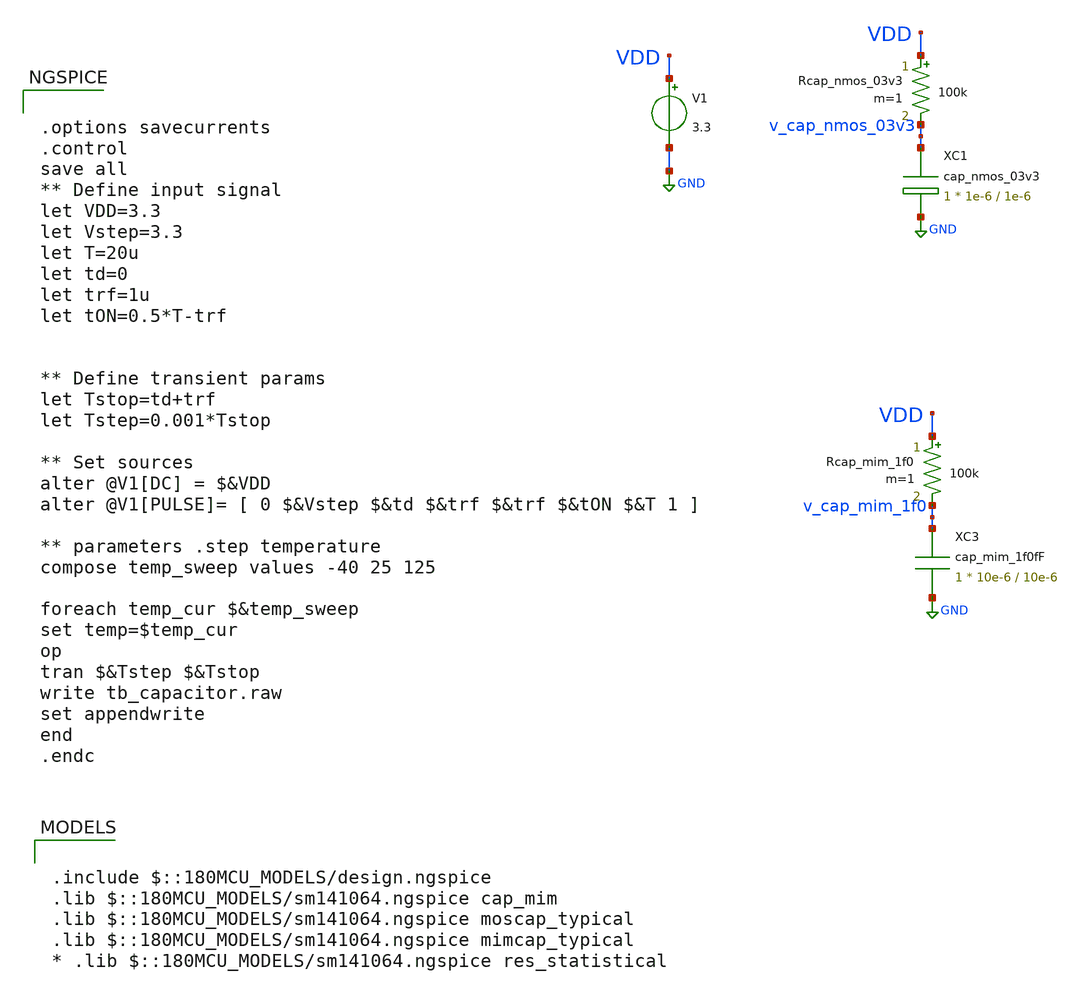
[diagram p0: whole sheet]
** sch_path: designs/libs/tb_analog/tb_capacitor/tb_capacitor.sch
**.subckt tb_capacitor
V1 VDD GND 3.3
XC1 v_cap_nmos_03v3 GND cap_nmos_03v3 c_width=1e-6 c_length=1e-6 m=1
Rcap_nmos_03v3 VDD v_cap_nmos_03v3 100k m=1
Rcap_mim_1f0 VDD v_cap_mim_1f0 100k m=1
XC3 v_cap_mim_1f0 GND cap_mim_1f0fF c_width=10e-6 c_length=10e-6 m=1
**** begin user architecture code

.include $::180MCU_MODELS/design.ngspice
.lib $::180MCU_MODELS/sm141064.ngspice cap_mim
.lib $::180MCU_MODELS/sm141064.ngspice moscap_typical
.lib $::180MCU_MODELS/sm141064.ngspice mimcap_typical
* .lib $::180MCU_MODELS/sm141064.ngspice res_statistical



.options savecurrents
.control
save all
** Define input signal
let VDD=3.3
let Vstep=3.3
let T=20u
let td=0
let trf=1u
let tON=0.5*T-trf


** Define transient params
let Tstop=td+trf
let Tstep=0.001*Tstop

** Set sources
alter @V1[DC] = $&VDD
alter @V1[PULSE]= [ 0 $&Vstep $&td $&trf $&trf $&tON $&T 1 ]

** parameters .step temperature
compose temp_sweep values -40 25 125

foreach temp_cur $&temp_sweep
set temp=$temp_cur
op
tran $&Tstep $&Tstop
write tb_capacitor.raw
set appendwrite
end
.endc


**** end user architecture code
**.ends
.GLOBAL GND
.end
